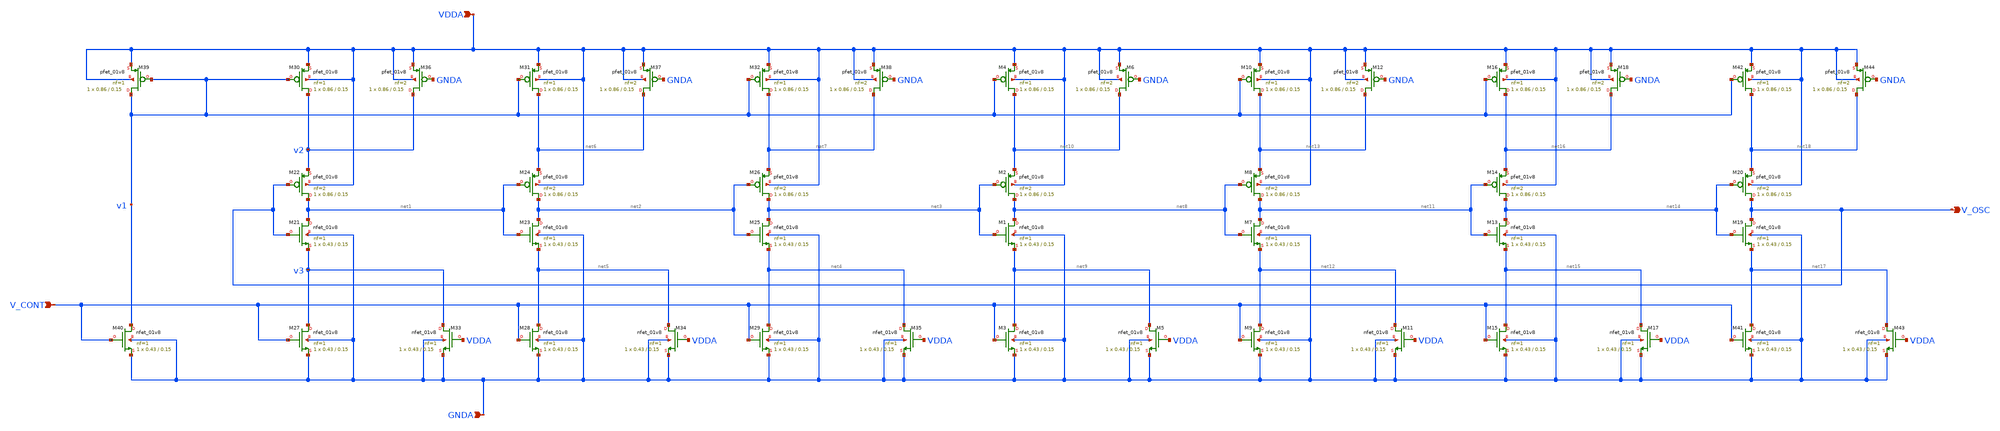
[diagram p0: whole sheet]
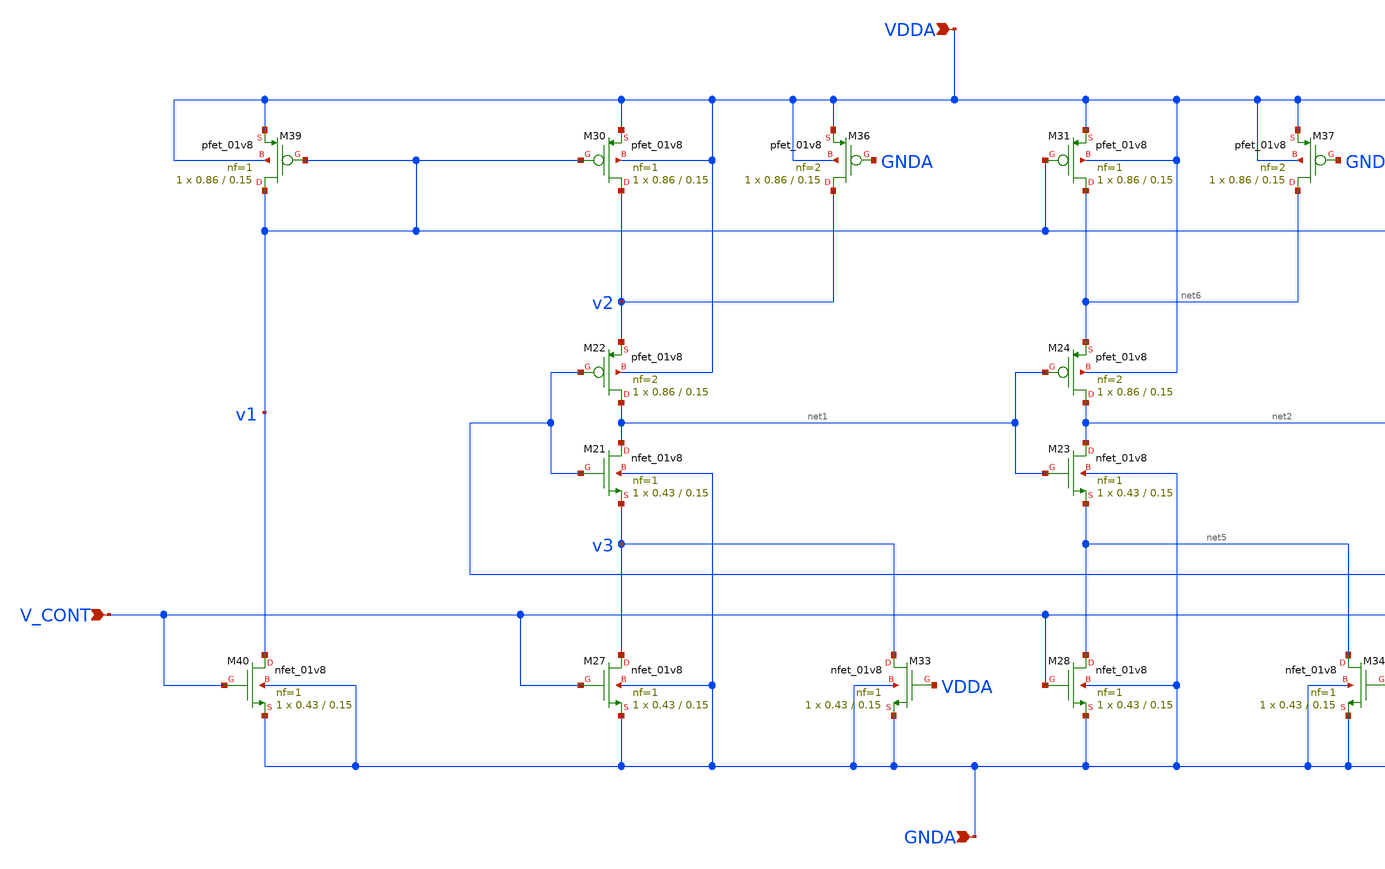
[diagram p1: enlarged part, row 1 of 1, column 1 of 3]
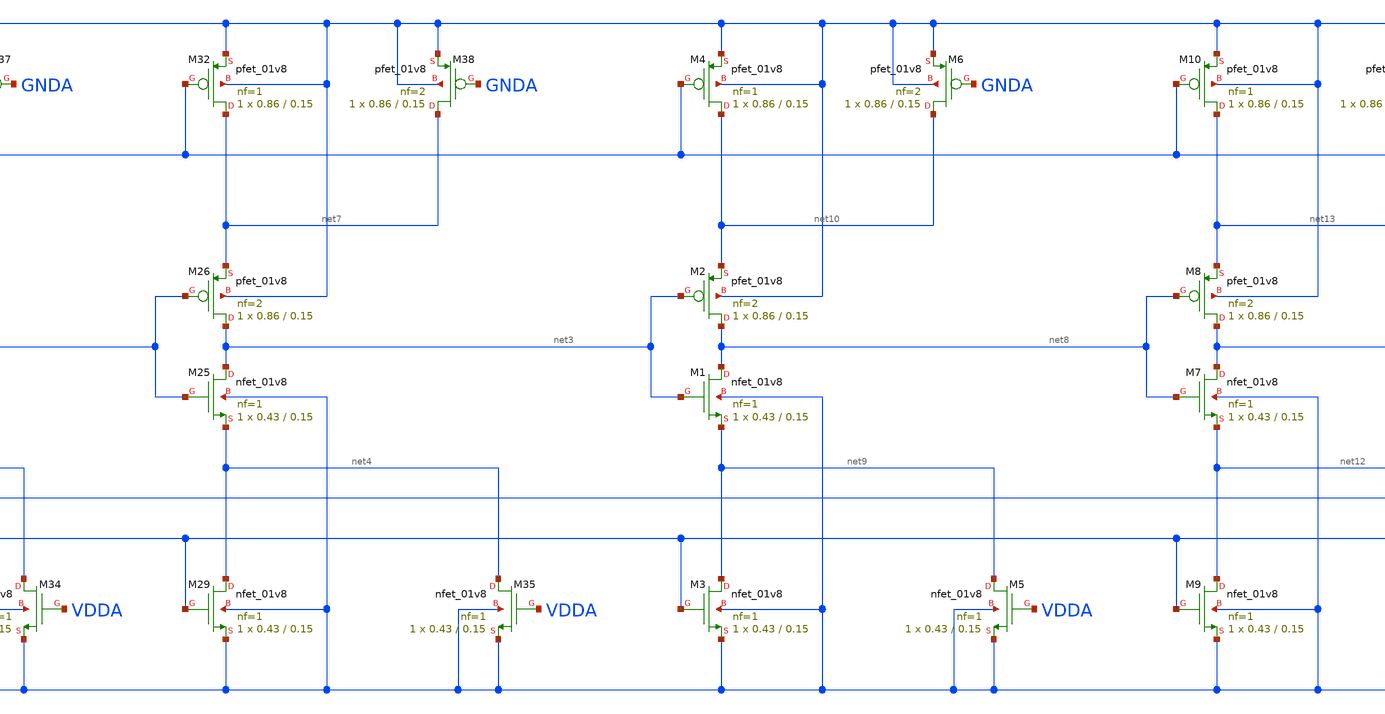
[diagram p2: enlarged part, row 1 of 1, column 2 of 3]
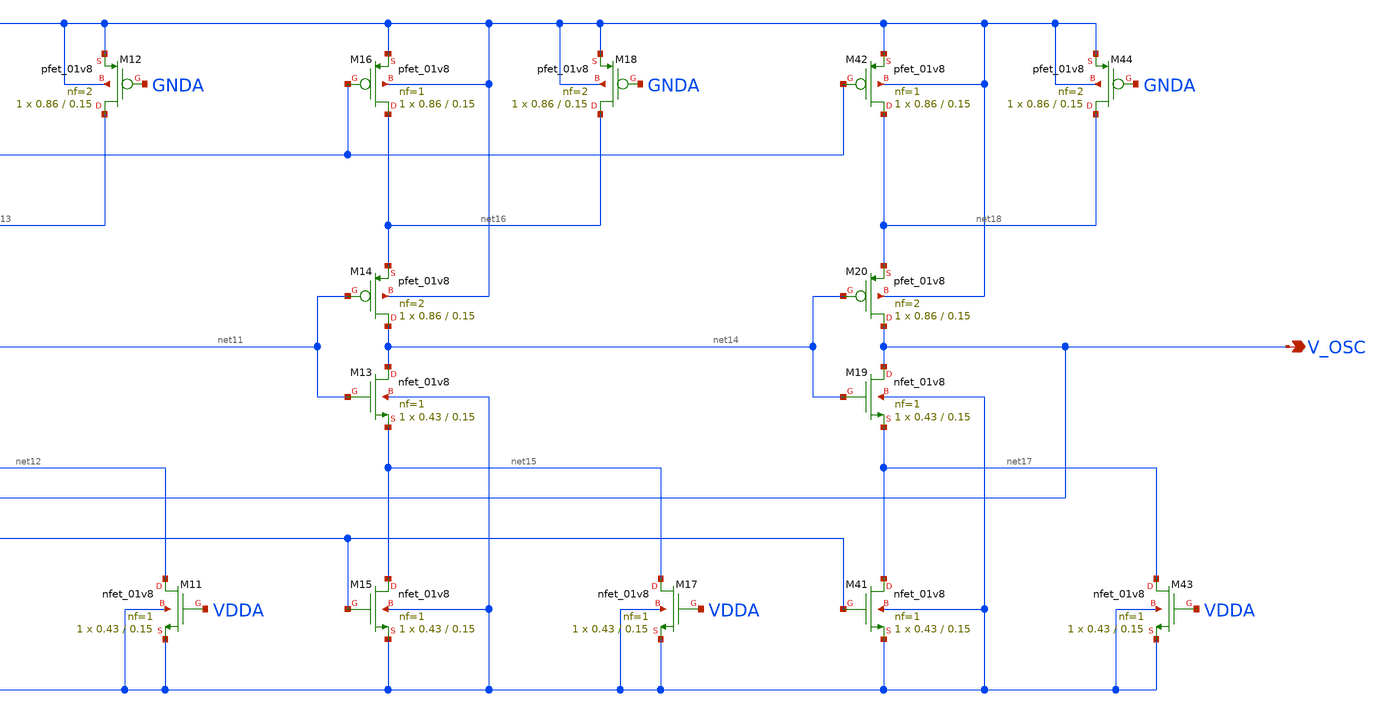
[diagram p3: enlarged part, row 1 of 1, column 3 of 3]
** sch_path: projects/pll/vco/xschem_ngspice/current_starved_VCO11.sch
**.subckt current_starved_VCO11 V_OSC VDDA GNDA V_CONT
*.opin V_OSC
*.ipin VDDA
*.ipin GNDA
*.ipin V_CONT
XM21 net1 V_OSC v3 GNDA sky130_fd_pr__nfet_01v8 L=0.15 W=0.43 nf=1 ad='int((nf+1)/2) * W/nf * 0.29' as='int((nf+2)/2) * W/nf * 0.29'
+ pd='2*int((nf+1)/2) * (W/nf + 0.29)' ps='2*int((nf+2)/2) * (W/nf + 0.29)' nrd='0.29 / W' nrs='0.29 / W'
+ sa=0 sb=0 sd=0 mult=1 m=1
XM22 net1 V_OSC v2 VDDA sky130_fd_pr__pfet_01v8 L=0.15 W=0.86 nf=2 ad='int((nf+1)/2) * W/nf * 0.29' as='int((nf+2)/2) * W/nf * 0.29'
+ pd='2*int((nf+1)/2) * (W/nf + 0.29)' ps='2*int((nf+2)/2) * (W/nf + 0.29)' nrd='0.29 / W' nrs='0.29 / W'
+ sa=0 sb=0 sd=0 mult=1 m=1
XM23 net2 net1 net5 GNDA sky130_fd_pr__nfet_01v8 L=0.15 W=0.43 nf=1 ad='int((nf+1)/2) * W/nf * 0.29'
+ as='int((nf+2)/2) * W/nf * 0.29' pd='2*int((nf+1)/2) * (W/nf + 0.29)' ps='2*int((nf+2)/2) * (W/nf + 0.29)'
+ nrd='0.29 / W' nrs='0.29 / W' sa=0 sb=0 sd=0 mult=1 m=1
XM24 net2 net1 net6 VDDA sky130_fd_pr__pfet_01v8 L=0.15 W=0.86 nf=2 ad='int((nf+1)/2) * W/nf * 0.29'
+ as='int((nf+2)/2) * W/nf * 0.29' pd='2*int((nf+1)/2) * (W/nf + 0.29)' ps='2*int((nf+2)/2) * (W/nf + 0.29)'
+ nrd='0.29 / W' nrs='0.29 / W' sa=0 sb=0 sd=0 mult=1 m=1
XM25 net3 net2 net4 GNDA sky130_fd_pr__nfet_01v8 L=0.15 W=0.43 nf=1 ad='int((nf+1)/2) * W/nf * 0.29'
+ as='int((nf+2)/2) * W/nf * 0.29' pd='2*int((nf+1)/2) * (W/nf + 0.29)' ps='2*int((nf+2)/2) * (W/nf + 0.29)'
+ nrd='0.29 / W' nrs='0.29 / W' sa=0 sb=0 sd=0 mult=1 m=1
XM26 net3 net2 net7 VDDA sky130_fd_pr__pfet_01v8 L=0.15 W=0.86 nf=2 ad='int((nf+1)/2) * W/nf * 0.29'
+ as='int((nf+2)/2) * W/nf * 0.29' pd='2*int((nf+1)/2) * (W/nf + 0.29)' ps='2*int((nf+2)/2) * (W/nf + 0.29)'
+ nrd='0.29 / W' nrs='0.29 / W' sa=0 sb=0 sd=0 mult=1 m=1
XM27 v3 V_CONT GNDA GNDA sky130_fd_pr__nfet_01v8 L=0.15 W=0.43 nf=1 ad='int((nf+1)/2) * W/nf * 0.29'
+ as='int((nf+2)/2) * W/nf * 0.29' pd='2*int((nf+1)/2) * (W/nf + 0.29)' ps='2*int((nf+2)/2) * (W/nf + 0.29)'
+ nrd='0.29 / W' nrs='0.29 / W' sa=0 sb=0 sd=0 mult=1 m=1
XM28 net5 V_CONT GNDA GNDA sky130_fd_pr__nfet_01v8 L=0.15 W=0.43 nf=1 ad='int((nf+1)/2) * W/nf * 0.29'
+ as='int((nf+2)/2) * W/nf * 0.29' pd='2*int((nf+1)/2) * (W/nf + 0.29)' ps='2*int((nf+2)/2) * (W/nf + 0.29)'
+ nrd='0.29 / W' nrs='0.29 / W' sa=0 sb=0 sd=0 mult=1 m=1
XM29 net4 V_CONT GNDA GNDA sky130_fd_pr__nfet_01v8 L=0.15 W=0.43 nf=1 ad='int((nf+1)/2) * W/nf * 0.29'
+ as='int((nf+2)/2) * W/nf * 0.29' pd='2*int((nf+1)/2) * (W/nf + 0.29)' ps='2*int((nf+2)/2) * (W/nf + 0.29)'
+ nrd='0.29 / W' nrs='0.29 / W' sa=0 sb=0 sd=0 mult=1 m=1
XM30 v2 v1 VDDA VDDA sky130_fd_pr__pfet_01v8 L=0.15 W=0.86 nf=1 ad='int((nf+1)/2) * W/nf * 0.29' as='int((nf+2)/2) * W/nf * 0.29'
+ pd='2*int((nf+1)/2) * (W/nf + 0.29)' ps='2*int((nf+2)/2) * (W/nf + 0.29)' nrd='0.29 / W' nrs='0.29 / W'
+ sa=0 sb=0 sd=0 mult=1 m=1
XM31 net6 v1 VDDA VDDA sky130_fd_pr__pfet_01v8 L=0.15 W=0.86 nf=1 ad='int((nf+1)/2) * W/nf * 0.29' as='int((nf+2)/2) * W/nf * 0.29'
+ pd='2*int((nf+1)/2) * (W/nf + 0.29)' ps='2*int((nf+2)/2) * (W/nf + 0.29)' nrd='0.29 / W' nrs='0.29 / W'
+ sa=0 sb=0 sd=0 mult=1 m=1
XM32 net7 v1 VDDA VDDA sky130_fd_pr__pfet_01v8 L=0.15 W=0.86 nf=1 ad='int((nf+1)/2) * W/nf * 0.29' as='int((nf+2)/2) * W/nf * 0.29'
+ pd='2*int((nf+1)/2) * (W/nf + 0.29)' ps='2*int((nf+2)/2) * (W/nf + 0.29)' nrd='0.29 / W' nrs='0.29 / W'
+ sa=0 sb=0 sd=0 mult=1 m=1
XM33 v3 VDDA GNDA GNDA sky130_fd_pr__nfet_01v8 L=0.15 W=0.43 nf=1 ad='int((nf+1)/2) * W/nf * 0.29' as='int((nf+2)/2) * W/nf * 0.29'
+ pd='2*int((nf+1)/2) * (W/nf + 0.29)' ps='2*int((nf+2)/2) * (W/nf + 0.29)' nrd='0.29 / W' nrs='0.29 / W'
+ sa=0 sb=0 sd=0 mult=1 m=1
XM34 net5 VDDA GNDA GNDA sky130_fd_pr__nfet_01v8 L=0.15 W=0.43 nf=1 ad='int((nf+1)/2) * W/nf * 0.29'
+ as='int((nf+2)/2) * W/nf * 0.29' pd='2*int((nf+1)/2) * (W/nf + 0.29)' ps='2*int((nf+2)/2) * (W/nf + 0.29)'
+ nrd='0.29 / W' nrs='0.29 / W' sa=0 sb=0 sd=0 mult=1 m=1
XM35 net4 VDDA GNDA GNDA sky130_fd_pr__nfet_01v8 L=0.15 W=0.43 nf=1 ad='int((nf+1)/2) * W/nf * 0.29'
+ as='int((nf+2)/2) * W/nf * 0.29' pd='2*int((nf+1)/2) * (W/nf + 0.29)' ps='2*int((nf+2)/2) * (W/nf + 0.29)'
+ nrd='0.29 / W' nrs='0.29 / W' sa=0 sb=0 sd=0 mult=1 m=1
XM36 v2 GNDA VDDA VDDA sky130_fd_pr__pfet_01v8 L=0.15 W=0.86 nf=2 ad='int((nf+1)/2) * W/nf * 0.29' as='int((nf+2)/2) * W/nf * 0.29'
+ pd='2*int((nf+1)/2) * (W/nf + 0.29)' ps='2*int((nf+2)/2) * (W/nf + 0.29)' nrd='0.29 / W' nrs='0.29 / W'
+ sa=0 sb=0 sd=0 mult=1 m=1
XM37 net6 GNDA VDDA VDDA sky130_fd_pr__pfet_01v8 L=0.15 W=0.86 nf=2 ad='int((nf+1)/2) * W/nf * 0.29'
+ as='int((nf+2)/2) * W/nf * 0.29' pd='2*int((nf+1)/2) * (W/nf + 0.29)' ps='2*int((nf+2)/2) * (W/nf + 0.29)'
+ nrd='0.29 / W' nrs='0.29 / W' sa=0 sb=0 sd=0 mult=1 m=1
XM38 net7 GNDA VDDA VDDA sky130_fd_pr__pfet_01v8 L=0.15 W=0.86 nf=2 ad='int((nf+1)/2) * W/nf * 0.29'
+ as='int((nf+2)/2) * W/nf * 0.29' pd='2*int((nf+1)/2) * (W/nf + 0.29)' ps='2*int((nf+2)/2) * (W/nf + 0.29)'
+ nrd='0.29 / W' nrs='0.29 / W' sa=0 sb=0 sd=0 mult=1 m=1
XM39 v1 v1 VDDA VDDA sky130_fd_pr__pfet_01v8 L=0.15 W=0.86 nf=1 ad='int((nf+1)/2) * W/nf * 0.29' as='int((nf+2)/2) * W/nf * 0.29'
+ pd='2*int((nf+1)/2) * (W/nf + 0.29)' ps='2*int((nf+2)/2) * (W/nf + 0.29)' nrd='0.29 / W' nrs='0.29 / W'
+ sa=0 sb=0 sd=0 mult=1 m=1
XM40 v1 V_CONT GNDA GNDA sky130_fd_pr__nfet_01v8 L=0.15 W=0.43 nf=1 ad='int((nf+1)/2) * W/nf * 0.29'
+ as='int((nf+2)/2) * W/nf * 0.29' pd='2*int((nf+1)/2) * (W/nf + 0.29)' ps='2*int((nf+2)/2) * (W/nf + 0.29)'
+ nrd='0.29 / W' nrs='0.29 / W' sa=0 sb=0 sd=0 mult=1 m=1
XM1 net8 net3 net9 GNDA sky130_fd_pr__nfet_01v8 L=0.15 W=0.43 nf=1 ad='int((nf+1)/2) * W/nf * 0.29' as='int((nf+2)/2) * W/nf * 0.29'
+ pd='2*int((nf+1)/2) * (W/nf + 0.29)' ps='2*int((nf+2)/2) * (W/nf + 0.29)' nrd='0.29 / W' nrs='0.29 / W'
+ sa=0 sb=0 sd=0 mult=1 m=1
XM2 net8 net3 net10 VDDA sky130_fd_pr__pfet_01v8 L=0.15 W=0.86 nf=2 ad='int((nf+1)/2) * W/nf * 0.29'
+ as='int((nf+2)/2) * W/nf * 0.29' pd='2*int((nf+1)/2) * (W/nf + 0.29)' ps='2*int((nf+2)/2) * (W/nf + 0.29)'
+ nrd='0.29 / W' nrs='0.29 / W' sa=0 sb=0 sd=0 mult=1 m=1
XM3 net9 V_CONT GNDA GNDA sky130_fd_pr__nfet_01v8 L=0.15 W=0.43 nf=1 ad='int((nf+1)/2) * W/nf * 0.29'
+ as='int((nf+2)/2) * W/nf * 0.29' pd='2*int((nf+1)/2) * (W/nf + 0.29)' ps='2*int((nf+2)/2) * (W/nf + 0.29)'
+ nrd='0.29 / W' nrs='0.29 / W' sa=0 sb=0 sd=0 mult=1 m=1
XM4 net10 v1 VDDA VDDA sky130_fd_pr__pfet_01v8 L=0.15 W=0.86 nf=1 ad='int((nf+1)/2) * W/nf * 0.29' as='int((nf+2)/2) * W/nf * 0.29'
+ pd='2*int((nf+1)/2) * (W/nf + 0.29)' ps='2*int((nf+2)/2) * (W/nf + 0.29)' nrd='0.29 / W' nrs='0.29 / W'
+ sa=0 sb=0 sd=0 mult=1 m=1
XM5 net9 VDDA GNDA GNDA sky130_fd_pr__nfet_01v8 L=0.15 W=0.43 nf=1 ad='int((nf+1)/2) * W/nf * 0.29' as='int((nf+2)/2) * W/nf * 0.29'
+ pd='2*int((nf+1)/2) * (W/nf + 0.29)' ps='2*int((nf+2)/2) * (W/nf + 0.29)' nrd='0.29 / W' nrs='0.29 / W'
+ sa=0 sb=0 sd=0 mult=1 m=1
XM6 net10 GNDA VDDA VDDA sky130_fd_pr__pfet_01v8 L=0.15 W=0.86 nf=2 ad='int((nf+1)/2) * W/nf * 0.29'
+ as='int((nf+2)/2) * W/nf * 0.29' pd='2*int((nf+1)/2) * (W/nf + 0.29)' ps='2*int((nf+2)/2) * (W/nf + 0.29)'
+ nrd='0.29 / W' nrs='0.29 / W' sa=0 sb=0 sd=0 mult=1 m=1
XM7 net11 net8 net12 GNDA sky130_fd_pr__nfet_01v8 L=0.15 W=0.43 nf=1 ad='int((nf+1)/2) * W/nf * 0.29'
+ as='int((nf+2)/2) * W/nf * 0.29' pd='2*int((nf+1)/2) * (W/nf + 0.29)' ps='2*int((nf+2)/2) * (W/nf + 0.29)'
+ nrd='0.29 / W' nrs='0.29 / W' sa=0 sb=0 sd=0 mult=1 m=1
XM8 net11 net8 net13 VDDA sky130_fd_pr__pfet_01v8 L=0.15 W=0.86 nf=2 ad='int((nf+1)/2) * W/nf * 0.29'
+ as='int((nf+2)/2) * W/nf * 0.29' pd='2*int((nf+1)/2) * (W/nf + 0.29)' ps='2*int((nf+2)/2) * (W/nf + 0.29)'
+ nrd='0.29 / W' nrs='0.29 / W' sa=0 sb=0 sd=0 mult=1 m=1
XM9 net12 V_CONT GNDA GNDA sky130_fd_pr__nfet_01v8 L=0.15 W=0.43 nf=1 ad='int((nf+1)/2) * W/nf * 0.29'
+ as='int((nf+2)/2) * W/nf * 0.29' pd='2*int((nf+1)/2) * (W/nf + 0.29)' ps='2*int((nf+2)/2) * (W/nf + 0.29)'
+ nrd='0.29 / W' nrs='0.29 / W' sa=0 sb=0 sd=0 mult=1 m=1
XM10 net13 v1 VDDA VDDA sky130_fd_pr__pfet_01v8 L=0.15 W=0.86 nf=1 ad='int((nf+1)/2) * W/nf * 0.29' as='int((nf+2)/2) * W/nf * 0.29'
+ pd='2*int((nf+1)/2) * (W/nf + 0.29)' ps='2*int((nf+2)/2) * (W/nf + 0.29)' nrd='0.29 / W' nrs='0.29 / W'
+ sa=0 sb=0 sd=0 mult=1 m=1
XM11 net12 VDDA GNDA GNDA sky130_fd_pr__nfet_01v8 L=0.15 W=0.43 nf=1 ad='int((nf+1)/2) * W/nf * 0.29'
+ as='int((nf+2)/2) * W/nf * 0.29' pd='2*int((nf+1)/2) * (W/nf + 0.29)' ps='2*int((nf+2)/2) * (W/nf + 0.29)'
+ nrd='0.29 / W' nrs='0.29 / W' sa=0 sb=0 sd=0 mult=1 m=1
XM12 net13 GNDA VDDA VDDA sky130_fd_pr__pfet_01v8 L=0.15 W=0.86 nf=2 ad='int((nf+1)/2) * W/nf * 0.29'
+ as='int((nf+2)/2) * W/nf * 0.29' pd='2*int((nf+1)/2) * (W/nf + 0.29)' ps='2*int((nf+2)/2) * (W/nf + 0.29)'
+ nrd='0.29 / W' nrs='0.29 / W' sa=0 sb=0 sd=0 mult=1 m=1
XM13 net14 net11 net15 GNDA sky130_fd_pr__nfet_01v8 L=0.15 W=0.43 nf=1 ad='int((nf+1)/2) * W/nf * 0.29'
+ as='int((nf+2)/2) * W/nf * 0.29' pd='2*int((nf+1)/2) * (W/nf + 0.29)' ps='2*int((nf+2)/2) * (W/nf + 0.29)'
+ nrd='0.29 / W' nrs='0.29 / W' sa=0 sb=0 sd=0 mult=1 m=1
XM14 net14 net11 net16 VDDA sky130_fd_pr__pfet_01v8 L=0.15 W=0.86 nf=2 ad='int((nf+1)/2) * W/nf * 0.29'
+ as='int((nf+2)/2) * W/nf * 0.29' pd='2*int((nf+1)/2) * (W/nf + 0.29)' ps='2*int((nf+2)/2) * (W/nf + 0.29)'
+ nrd='0.29 / W' nrs='0.29 / W' sa=0 sb=0 sd=0 mult=1 m=1
XM15 net15 V_CONT GNDA GNDA sky130_fd_pr__nfet_01v8 L=0.15 W=0.43 nf=1 ad='int((nf+1)/2) * W/nf * 0.29'
+ as='int((nf+2)/2) * W/nf * 0.29' pd='2*int((nf+1)/2) * (W/nf + 0.29)' ps='2*int((nf+2)/2) * (W/nf + 0.29)'
+ nrd='0.29 / W' nrs='0.29 / W' sa=0 sb=0 sd=0 mult=1 m=1
XM16 net16 v1 VDDA VDDA sky130_fd_pr__pfet_01v8 L=0.15 W=0.86 nf=1 ad='int((nf+1)/2) * W/nf * 0.29' as='int((nf+2)/2) * W/nf * 0.29'
+ pd='2*int((nf+1)/2) * (W/nf + 0.29)' ps='2*int((nf+2)/2) * (W/nf + 0.29)' nrd='0.29 / W' nrs='0.29 / W'
+ sa=0 sb=0 sd=0 mult=1 m=1
XM17 net15 VDDA GNDA GNDA sky130_fd_pr__nfet_01v8 L=0.15 W=0.43 nf=1 ad='int((nf+1)/2) * W/nf * 0.29'
+ as='int((nf+2)/2) * W/nf * 0.29' pd='2*int((nf+1)/2) * (W/nf + 0.29)' ps='2*int((nf+2)/2) * (W/nf + 0.29)'
+ nrd='0.29 / W' nrs='0.29 / W' sa=0 sb=0 sd=0 mult=1 m=1
XM18 net16 GNDA VDDA VDDA sky130_fd_pr__pfet_01v8 L=0.15 W=0.86 nf=2 ad='int((nf+1)/2) * W/nf * 0.29'
+ as='int((nf+2)/2) * W/nf * 0.29' pd='2*int((nf+1)/2) * (W/nf + 0.29)' ps='2*int((nf+2)/2) * (W/nf + 0.29)'
+ nrd='0.29 / W' nrs='0.29 / W' sa=0 sb=0 sd=0 mult=1 m=1
XM19 V_OSC net14 net17 GNDA sky130_fd_pr__nfet_01v8 L=0.15 W=0.43 nf=1 ad='int((nf+1)/2) * W/nf * 0.29'
+ as='int((nf+2)/2) * W/nf * 0.29' pd='2*int((nf+1)/2) * (W/nf + 0.29)' ps='2*int((nf+2)/2) * (W/nf + 0.29)'
+ nrd='0.29 / W' nrs='0.29 / W' sa=0 sb=0 sd=0 mult=1 m=1
XM20 V_OSC net14 net18 VDDA sky130_fd_pr__pfet_01v8 L=0.15 W=0.86 nf=2 ad='int((nf+1)/2) * W/nf * 0.29'
+ as='int((nf+2)/2) * W/nf * 0.29' pd='2*int((nf+1)/2) * (W/nf + 0.29)' ps='2*int((nf+2)/2) * (W/nf + 0.29)'
+ nrd='0.29 / W' nrs='0.29 / W' sa=0 sb=0 sd=0 mult=1 m=1
XM41 net17 V_CONT GNDA GNDA sky130_fd_pr__nfet_01v8 L=0.15 W=0.43 nf=1 ad='int((nf+1)/2) * W/nf * 0.29'
+ as='int((nf+2)/2) * W/nf * 0.29' pd='2*int((nf+1)/2) * (W/nf + 0.29)' ps='2*int((nf+2)/2) * (W/nf + 0.29)'
+ nrd='0.29 / W' nrs='0.29 / W' sa=0 sb=0 sd=0 mult=1 m=1
XM42 net18 v1 VDDA VDDA sky130_fd_pr__pfet_01v8 L=0.15 W=0.86 nf=1 ad='int((nf+1)/2) * W/nf * 0.29' as='int((nf+2)/2) * W/nf * 0.29'
+ pd='2*int((nf+1)/2) * (W/nf + 0.29)' ps='2*int((nf+2)/2) * (W/nf + 0.29)' nrd='0.29 / W' nrs='0.29 / W'
+ sa=0 sb=0 sd=0 mult=1 m=1
XM43 net17 VDDA GNDA GNDA sky130_fd_pr__nfet_01v8 L=0.15 W=0.43 nf=1 ad='int((nf+1)/2) * W/nf * 0.29'
+ as='int((nf+2)/2) * W/nf * 0.29' pd='2*int((nf+1)/2) * (W/nf + 0.29)' ps='2*int((nf+2)/2) * (W/nf + 0.29)'
+ nrd='0.29 / W' nrs='0.29 / W' sa=0 sb=0 sd=0 mult=1 m=1
XM44 net18 GNDA VDDA VDDA sky130_fd_pr__pfet_01v8 L=0.15 W=0.86 nf=2 ad='int((nf+1)/2) * W/nf * 0.29'
+ as='int((nf+2)/2) * W/nf * 0.29' pd='2*int((nf+1)/2) * (W/nf + 0.29)' ps='2*int((nf+2)/2) * (W/nf + 0.29)'
+ nrd='0.29 / W' nrs='0.29 / W' sa=0 sb=0 sd=0 mult=1 m=1
**.ends
.end
